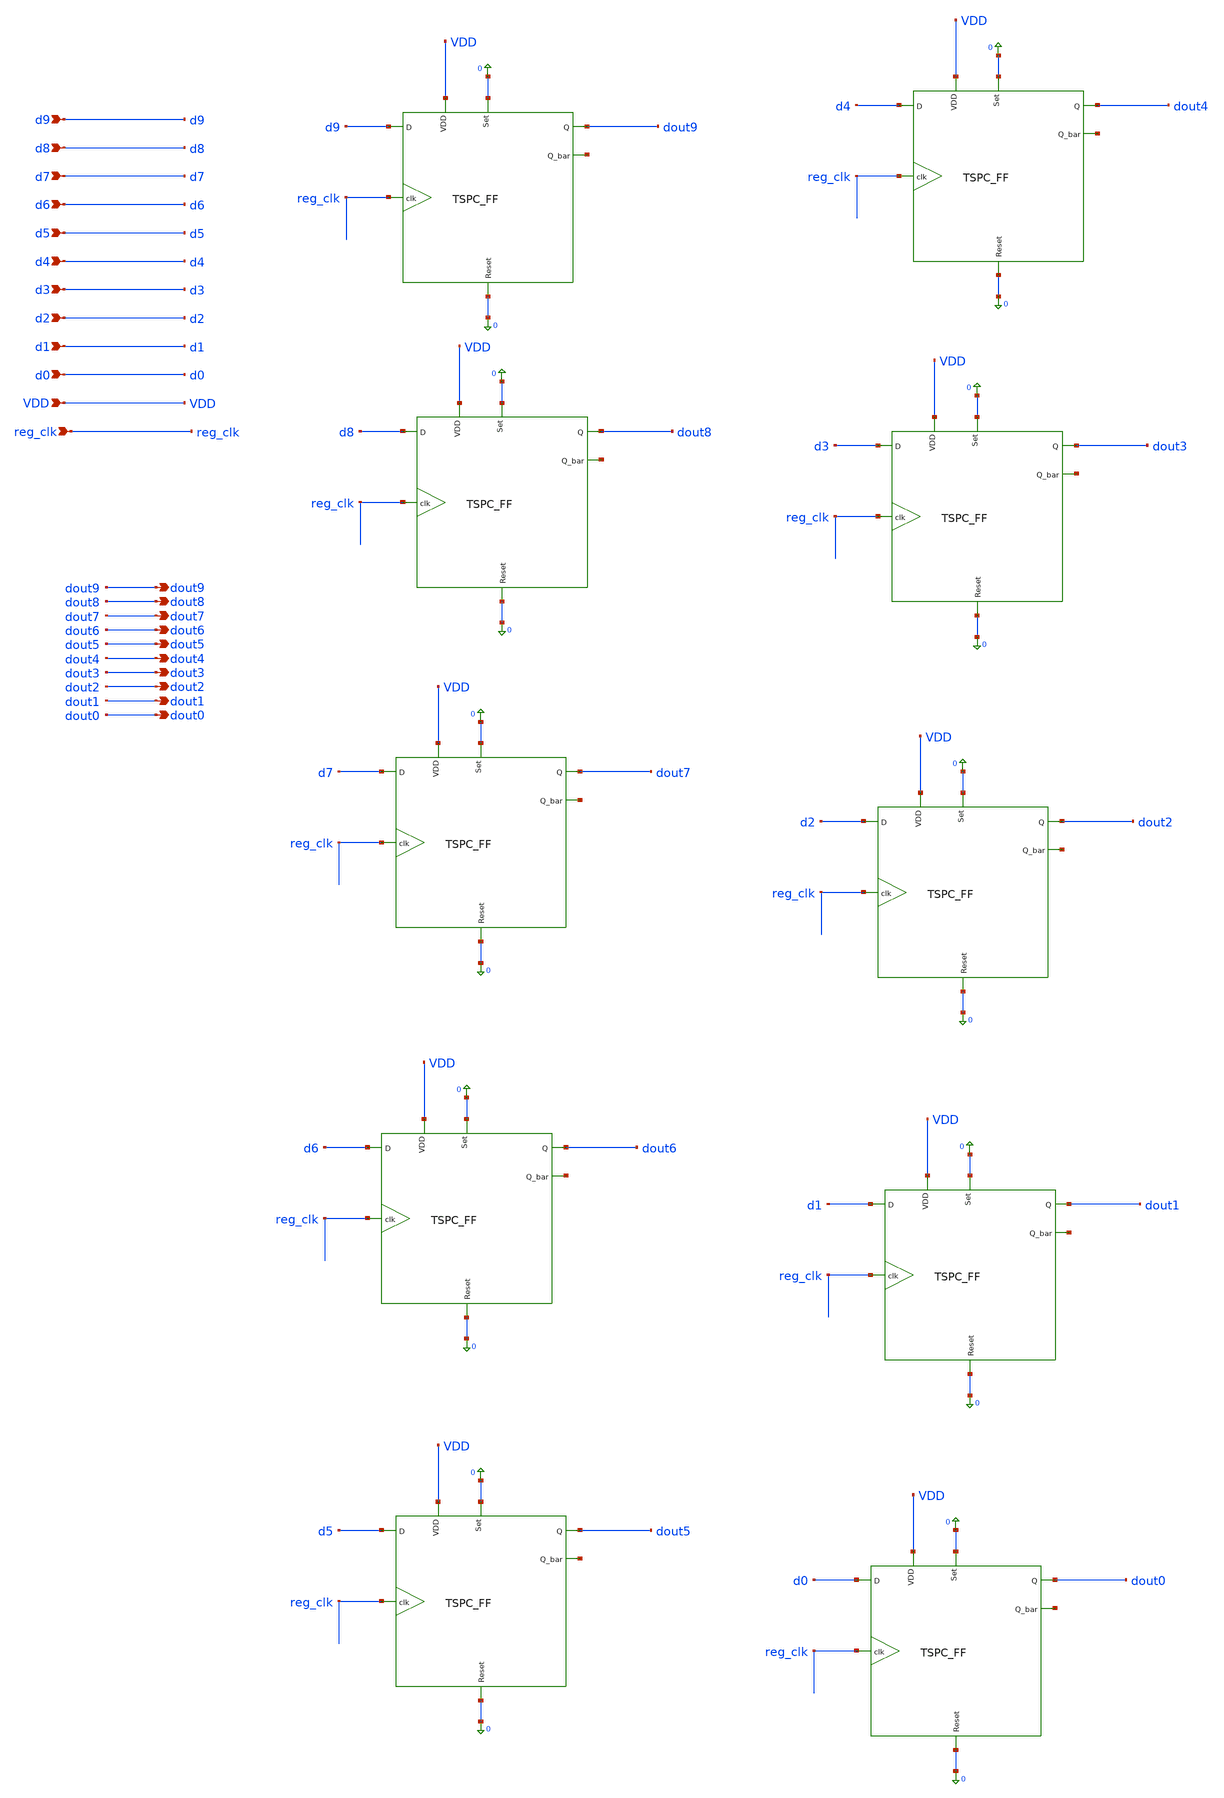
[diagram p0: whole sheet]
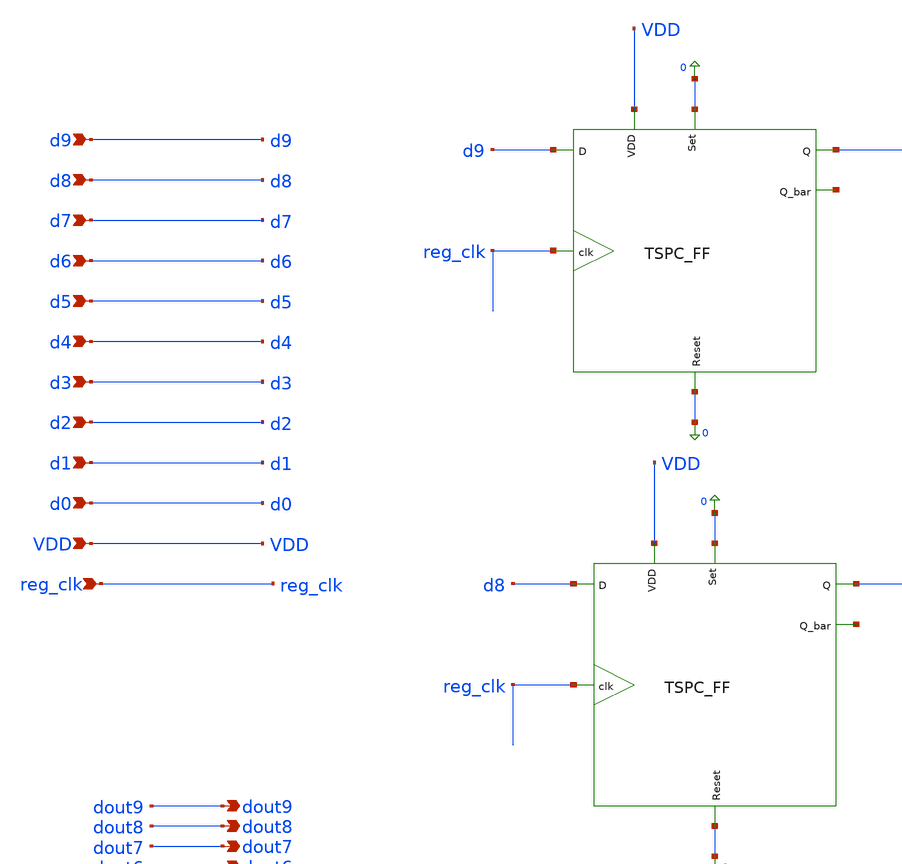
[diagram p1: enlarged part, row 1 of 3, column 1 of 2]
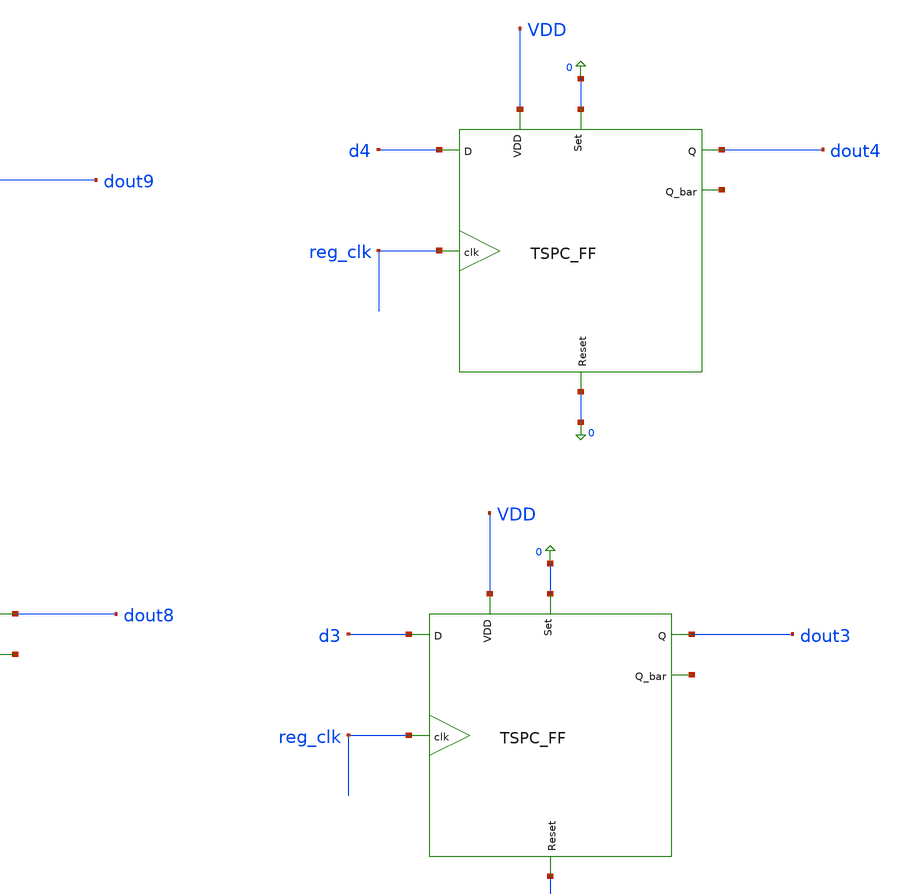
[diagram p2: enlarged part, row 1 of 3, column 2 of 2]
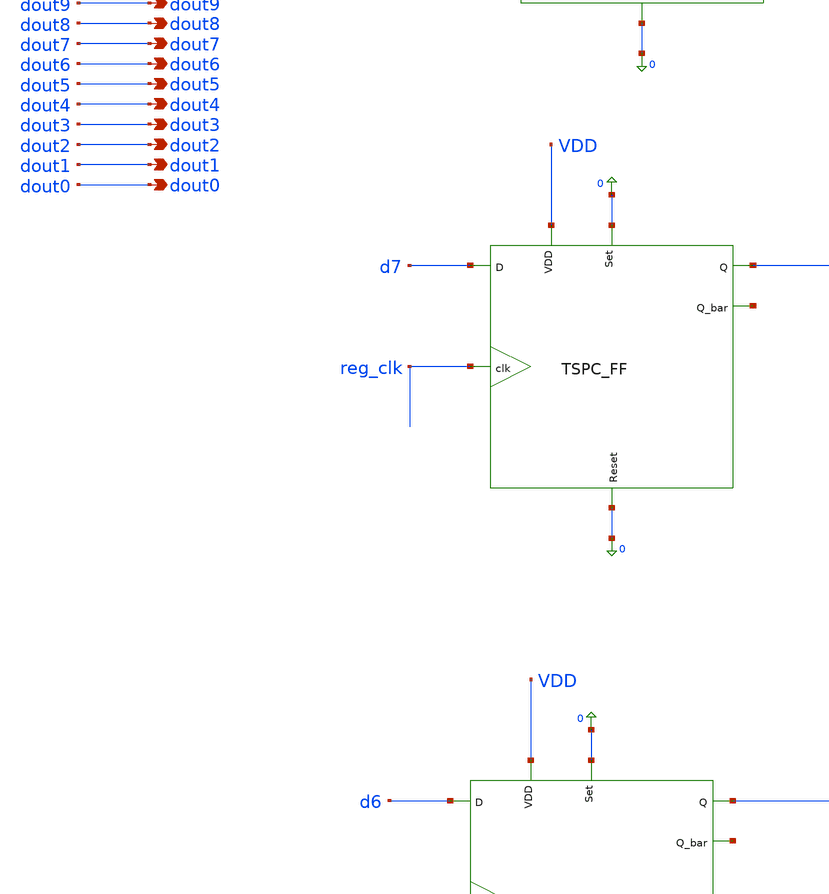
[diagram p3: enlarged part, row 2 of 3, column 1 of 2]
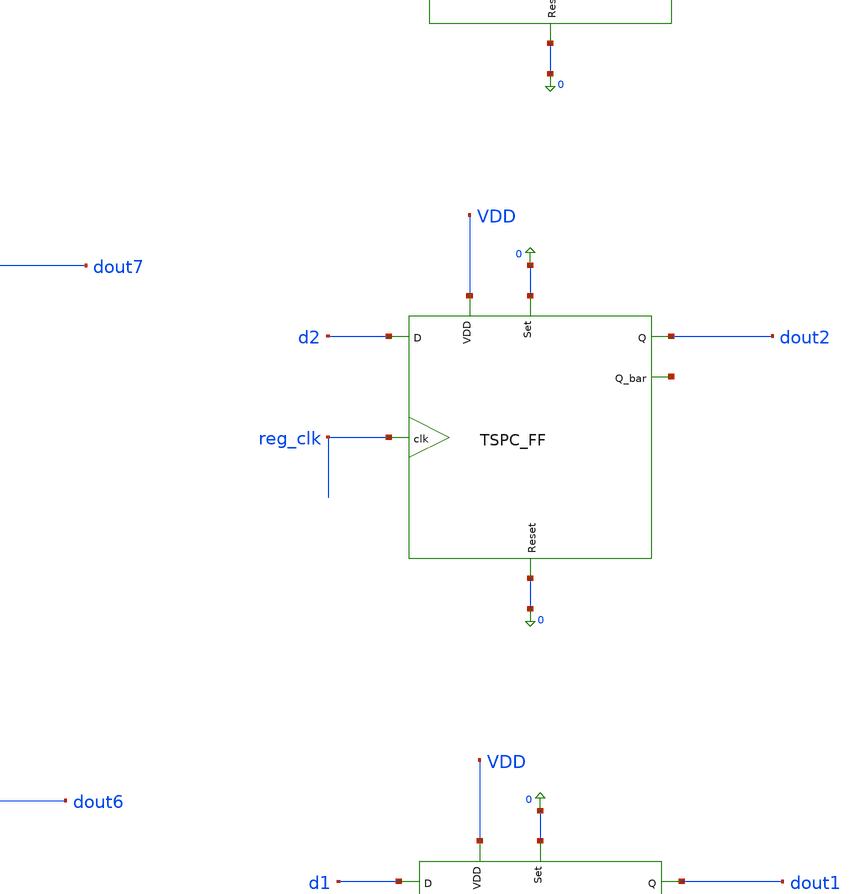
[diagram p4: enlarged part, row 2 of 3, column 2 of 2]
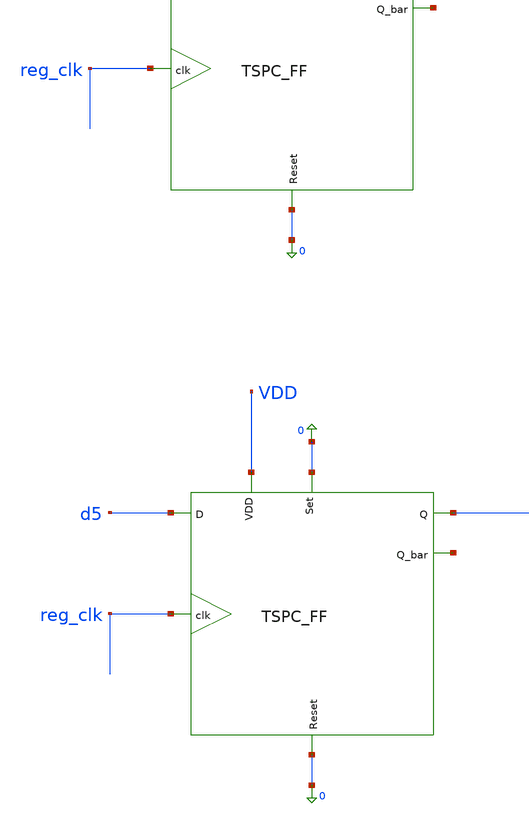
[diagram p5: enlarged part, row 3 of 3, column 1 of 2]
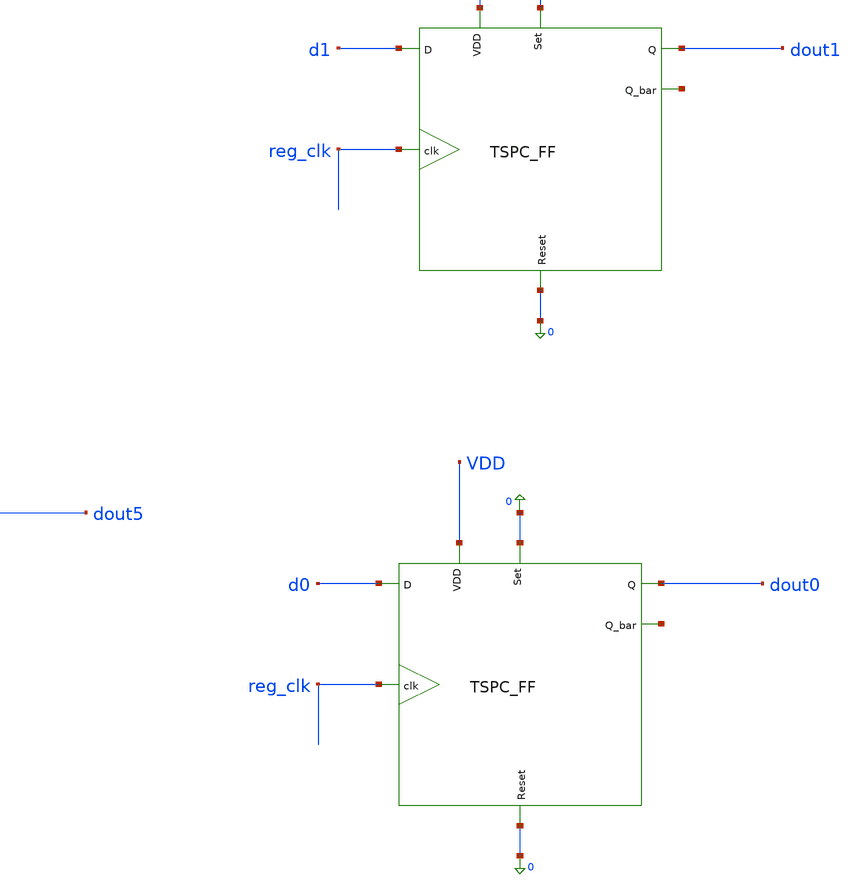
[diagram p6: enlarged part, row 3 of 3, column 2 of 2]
** sch_path: Design_Files/IC Design/Schematic/SAR_ADC_BLOCKS/OUT_REG/OUT_REG.sch
**.subckt OUT_REG VDD reg_clk dout9 dout8 dout7 dout6 dout5 dout4 dout3 dout2 dout1 dout0 d9 d8 d7
*+ d6 d5 d4 d3 d2 d1 d0
*.ipin VDD
*.ipin reg_clk
*.opin dout9
*.opin dout8
*.opin dout7
*.opin dout6
*.opin dout5
*.opin dout4
*.opin dout3
*.opin dout2
*.opin dout1
*.opin dout0
*.ipin d9
*.ipin d8
*.ipin d7
*.ipin d6
*.ipin d5
*.ipin d4
*.ipin d3
*.ipin d2
*.ipin d1
*.ipin d0
xTSPCFF1 d9 reg_clk VDD 0 0 dout9 net1 TSPC_FF
xTSPCFF2 d4 reg_clk VDD 0 0 dout4 net2 TSPC_FF
xTSPCFF3 d8 reg_clk VDD 0 0 dout8 net3 TSPC_FF
xTSPCFF4 d3 reg_clk VDD 0 0 dout3 net4 TSPC_FF
xTSPCFF5 d7 reg_clk VDD 0 0 dout7 net5 TSPC_FF
xTSPCFF6 d2 reg_clk VDD 0 0 dout2 net6 TSPC_FF
xTSPCFF7 d6 reg_clk VDD 0 0 dout6 net7 TSPC_FF
xTSPCFF8 d1 reg_clk VDD 0 0 dout1 net8 TSPC_FF
xTSPCFF9 d5 reg_clk VDD 0 0 dout5 net9 TSPC_FF
xTSPCFF10 d0 reg_clk VDD 0 0 dout0 net10 TSPC_FF
**.ends

* expanding   symbol:  ECG_Acquisition_IC/Design_Files/IC
*+ Design/Schematic/SAR_ADC_BLOCKS/TSPC_FF/TSPC_FF.sym # of pins=7
** sym_path: Design_Files/IC Design/Schematic/SAR_ADC_BLOCKS/TSPC_FF/TSPC_FF.sym
** sch_path: Design_Files/IC Design/Schematic/SAR_ADC_BLOCKS/TSPC_FF/TSPC_FF.sch
.subckt TSPC_FF D clk VDD Set Reset Q Q_bar
*.ipin D
*.ipin clk
*.ipin VDD
*.ipin Set
*.ipin Reset
*.opin Q
*.opin Q_bar
XM1 net1 D VDD VDD pfet_03v3 L=0.28u W=5.10u nf=1 ad='int((nf+1)/2) * W/nf * 0.18u' as='int((nf+2)/2) * W/nf * 0.18u'
+ pd='2*int((nf+1)/2) * (W/nf + 0.18u)' ps='2*int((nf+2)/2) * (W/nf + 0.18u)' nrd='0.18u / W' nrs='0.18u / W'
+ sa=0 sb=0 sd=0 m=1
XM2 Q_1st clk net1 VDD pfet_03v3 L=0.28u W=6.12u nf=1 ad='int((nf+1)/2) * W/nf * 0.18u' as='int((nf+2)/2) * W/nf * 0.18u'
+ pd='2*int((nf+1)/2) * (W/nf + 0.18u)' ps='2*int((nf+2)/2) * (W/nf + 0.18u)' nrd='0.18u / W' nrs='0.18u / W'
+ sa=0 sb=0 sd=0 m=1
XM3 Q_1st D 0 0 nfet_03v3 L=0.28u W=1u nf=1 ad='int((nf+1)/2) * W/nf * 0.18u' as='int((nf+2)/2) * W/nf * 0.18u'
+ pd='2*int((nf+1)/2) * (W/nf + 0.18u)' ps='2*int((nf+2)/2) * (W/nf + 0.18u)' nrd='0.18u / W' nrs='0.18u / W'
+ sa=0 sb=0 sd=0 m=1
XM4 Q_pre clk VDD VDD pfet_03v3 L=0.28u W=10u nf=1 ad='int((nf+1)/2) * W/nf * 0.18u' as='int((nf+2)/2) * W/nf * 0.18u'
+ pd='2*int((nf+1)/2) * (W/nf + 0.18u)' ps='2*int((nf+2)/2) * (W/nf + 0.18u)' nrd='0.18u / W' nrs='0.18u / W'
+ sa=0 sb=0 sd=0 m=1
XM6 net2 clk 0 0 nfet_03v3 L=0.28u W=4u nf=1 ad='int((nf+1)/2) * W/nf * 0.18u' as='int((nf+2)/2) * W/nf * 0.18u'
+ pd='2*int((nf+1)/2) * (W/nf + 0.18u)' ps='2*int((nf+2)/2) * (W/nf + 0.18u)' nrd='0.18u / W' nrs='0.18u / W'
+ sa=0 sb=0 sd=0 m=1
XM7 net3 Q_pre VDD VDD pfet_03v3 L=0.28u W=5.10u nf=1 ad='int((nf+1)/2) * W/nf * 0.18u' as='int((nf+2)/2) * W/nf * 0.18u'
+ pd='2*int((nf+1)/2) * (W/nf + 0.18u)' ps='2*int((nf+2)/2) * (W/nf + 0.18u)' nrd='0.18u / W' nrs='0.18u / W'
+ sa=0 sb=0 sd=0 m=1
XM8 Q_bar_pre Set net3 VDD pfet_03v3 L=0.28u W=6.12u nf=1 ad='int((nf+1)/2) * W/nf * 0.18u' as='int((nf+2)/2) * W/nf * 0.18u'
+ pd='2*int((nf+1)/2) * (W/nf + 0.18u)' ps='2*int((nf+2)/2) * (W/nf + 0.18u)' nrd='0.18u / W' nrs='0.18u / W'
+ sa=0 sb=0 sd=0 m=1
XM9 Q_bar_pre clk net4 0 nfet_03v3 L=0.28u W=1.72u nf=1 ad='int((nf+1)/2) * W/nf * 0.18u' as='int((nf+2)/2) * W/nf * 0.18u'
+ pd='2*int((nf+1)/2) * (W/nf + 0.18u)' ps='2*int((nf+2)/2) * (W/nf + 0.18u)' nrd='0.18u / W' nrs='0.18u / W'
+ sa=0 sb=0 sd=0 m=1
XM10 net4 Q_pre net6 0 nfet_03v3 L=0.28u W=1.5u nf=1 ad='int((nf+1)/2) * W/nf * 0.18u' as='int((nf+2)/2) * W/nf * 0.18u'
+ pd='2*int((nf+1)/2) * (W/nf + 0.18u)' ps='2*int((nf+2)/2) * (W/nf + 0.18u)' nrd='0.18u / W' nrs='0.18u / W'
+ sa=0 sb=0 sd=0 m=1
XM11 Q_bar_pre net5 VDD VDD pfet_03v3 L=0.28u W=2u nf=1 ad='int((nf+1)/2) * W/nf * 0.18u' as='int((nf+2)/2) * W/nf * 0.18u'
+ pd='2*int((nf+1)/2) * (W/nf + 0.18u)' ps='2*int((nf+2)/2) * (W/nf + 0.18u)' nrd='0.18u / W' nrs='0.18u / W'
+ sa=0 sb=0 sd=0 m=1
XM12 Q_bar_pre Set 0 0 nfet_03v3 L=0.28u W=0.25u nf=1 ad='int((nf+1)/2) * W/nf * 0.18u' as='int((nf+2)/2) * W/nf * 0.18u'
+ pd='2*int((nf+1)/2) * (W/nf + 0.18u)' ps='2*int((nf+2)/2) * (W/nf + 0.18u)' nrd='0.18u / W' nrs='0.18u / W'
+ sa=0 sb=0 sd=0 m=1
XM13 Q Q_bar_pre VDD VDD pfet_03v3 L=0.28u W=0.425u nf=1 ad='int((nf+1)/2) * W/nf * 0.18u' as='int((nf+2)/2) * W/nf * 0.18u'
+ pd='2*int((nf+1)/2) * (W/nf + 0.18u)' ps='2*int((nf+2)/2) * (W/nf + 0.18u)' nrd='0.18u / W' nrs='0.18u / W'
+ sa=0 sb=0 sd=0 m=1
XM14 Q Q_bar_pre 0 0 nfet_03v3 L=0.56u W=0.5u nf=1 ad='int((nf+1)/2) * W/nf * 0.18u' as='int((nf+2)/2) * W/nf * 0.18u'
+ pd='2*int((nf+1)/2) * (W/nf + 0.18u)' ps='2*int((nf+2)/2) * (W/nf + 0.18u)' nrd='0.18u / W' nrs='0.18u / W'
+ sa=0 sb=0 sd=0 m=1
XM15 Q_bar Q VDD VDD pfet_03v3 L=0.28u W=0.22u nf=1 ad='int((nf+1)/2) * W/nf * 0.18u' as='int((nf+2)/2) * W/nf * 0.18u'
+ pd='2*int((nf+1)/2) * (W/nf + 0.18u)' ps='2*int((nf+2)/2) * (W/nf + 0.18u)' nrd='0.18u / W' nrs='0.18u / W'
+ sa=0 sb=0 sd=0 m=1
XM16 Q_bar Q 0 0 nfet_03v3 L=0.28u W=0.22u nf=1 ad='int((nf+1)/2) * W/nf * 0.18u' as='int((nf+2)/2) * W/nf * 0.18u'
+ pd='2*int((nf+1)/2) * (W/nf + 0.18u)' ps='2*int((nf+2)/2) * (W/nf + 0.18u)' nrd='0.18u / W' nrs='0.18u / W'
+ sa=0 sb=0 sd=0 m=1
XM17 net6 net7 0 0 nfet_03v3 L=0.28u W=1.5u nf=1 ad='int((nf+1)/2) * W/nf * 0.18u' as='int((nf+2)/2) * W/nf * 0.18u'
+ pd='2*int((nf+1)/2) * (W/nf + 0.18u)' ps='2*int((nf+2)/2) * (W/nf + 0.18u)' nrd='0.18u / W' nrs='0.18u / W'
+ sa=0 sb=0 sd=0 m=1
xINV1_1 Reset VDD net7 INV
xINV1_2 Reset VDD net5 INV
XM5 Q_pre Q_1st net2 0 nfet_03v3 L=0.28u W=4u nf=1 ad='int((nf+1)/2) * W/nf * 0.18u' as='int((nf+2)/2) * W/nf * 0.18u'
+ pd='2*int((nf+1)/2) * (W/nf + 0.18u)' ps='2*int((nf+2)/2) * (W/nf + 0.18u)' nrd='0.18u / W' nrs='0.18u / W'
+ sa=0 sb=0 sd=0 m=1
.ends


* expanding   symbol:  ECG_Acquisition_IC/Design_Files/IC
*+ Design/Schematic/SAR_ADC_BLOCKS/INV/INV.sym # of pins=3
** sym_path: Design_Files/IC Design/Schematic/SAR_ADC_BLOCKS/INV/INV.sym
** sch_path: Design_Files/IC Design/Schematic/SAR_ADC_BLOCKS/INV/INV.sch
.subckt INV in VDD out
*.ipin in
*.ipin VDD
*.opin out
XM1 out in 0 0 nfet_03v3 L=0.28u W=0.22u nf=1 ad='int((nf+1)/2) * W/nf * 0.18u' as='int((nf+2)/2) * W/nf * 0.18u'
+ pd='2*int((nf+1)/2) * (W/nf + 0.18u)' ps='2*int((nf+2)/2) * (W/nf + 0.18u)' nrd='0.18u / W' nrs='0.18u / W'
+ sa=0 sb=0 sd=0 m=wn_inv
XM2 out in vdd vdd pfet_03v3 L=0.28u W=0.22u nf=1 ad='int((nf+1)/2) * W/nf * 0.18u' as='int((nf+2)/2) * W/nf * 0.18u'
+ pd='2*int((nf+1)/2) * (W/nf + 0.18u)' ps='2*int((nf+2)/2) * (W/nf + 0.18u)' nrd='0.18u / W' nrs='0.18u / W'
+ sa=0 sb=0 sd=0 m=wp_inv
.ends

.end
